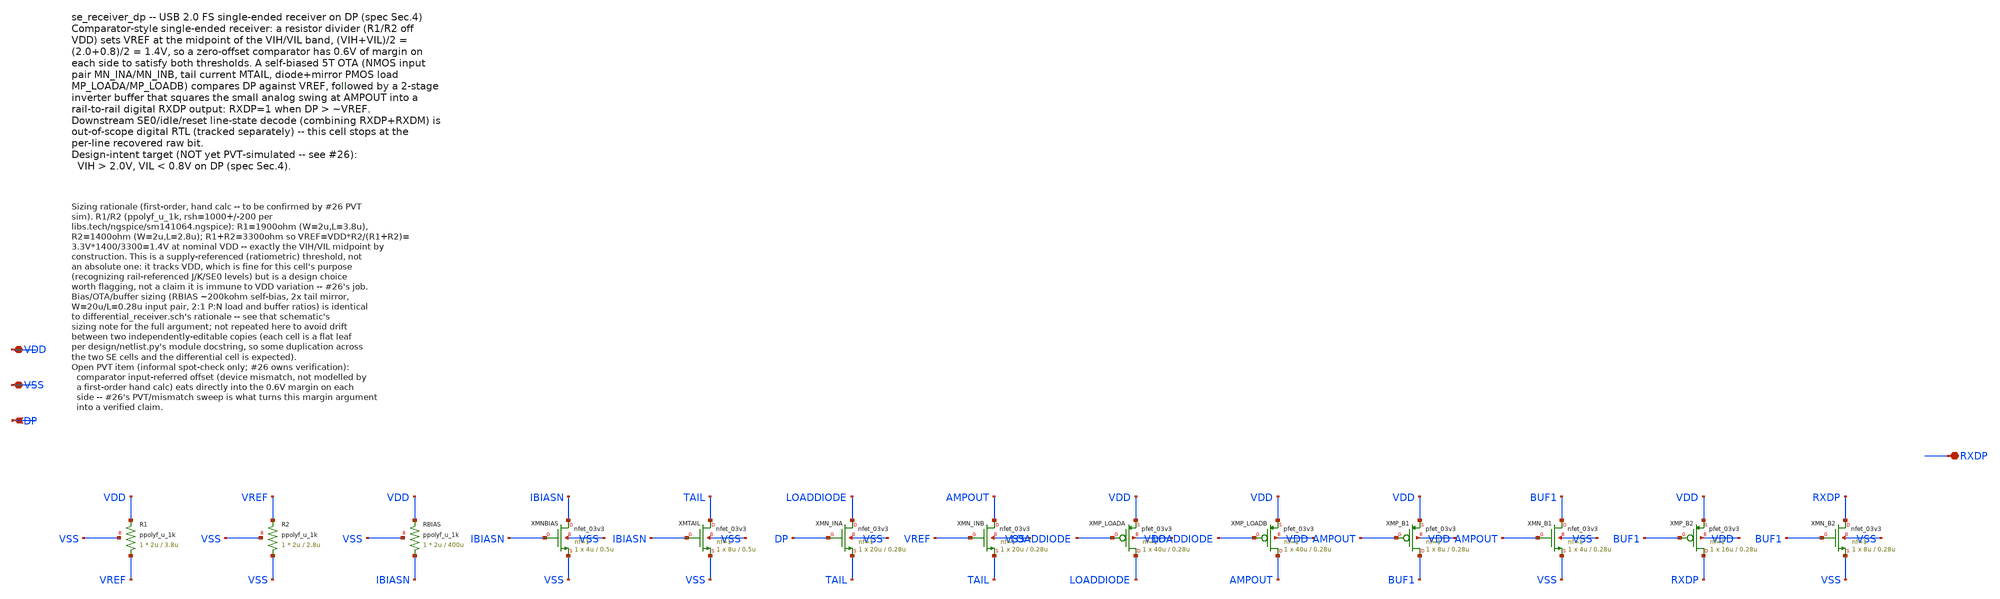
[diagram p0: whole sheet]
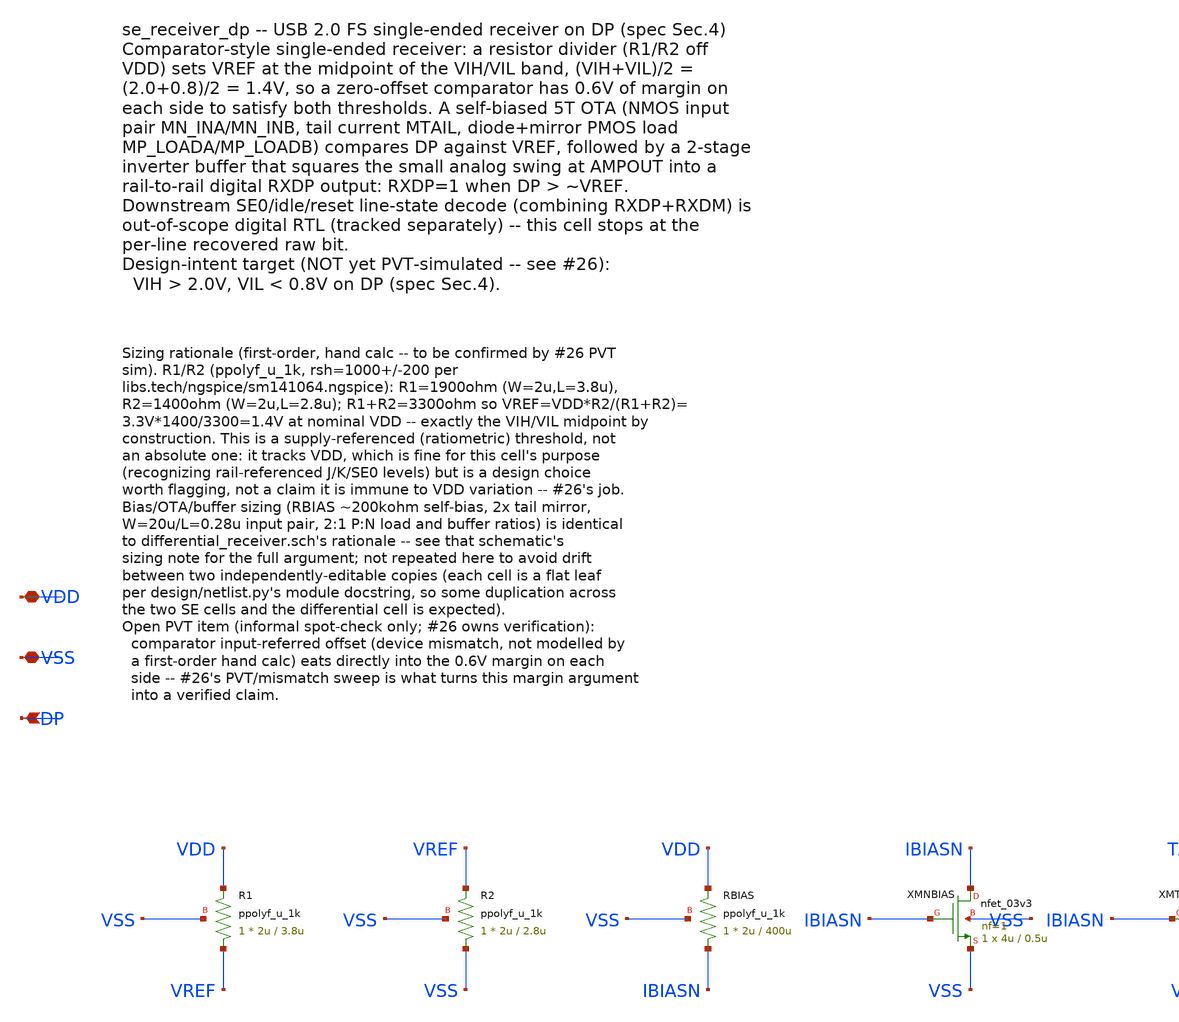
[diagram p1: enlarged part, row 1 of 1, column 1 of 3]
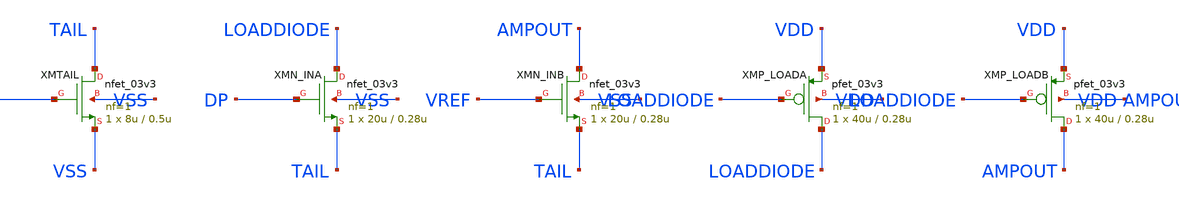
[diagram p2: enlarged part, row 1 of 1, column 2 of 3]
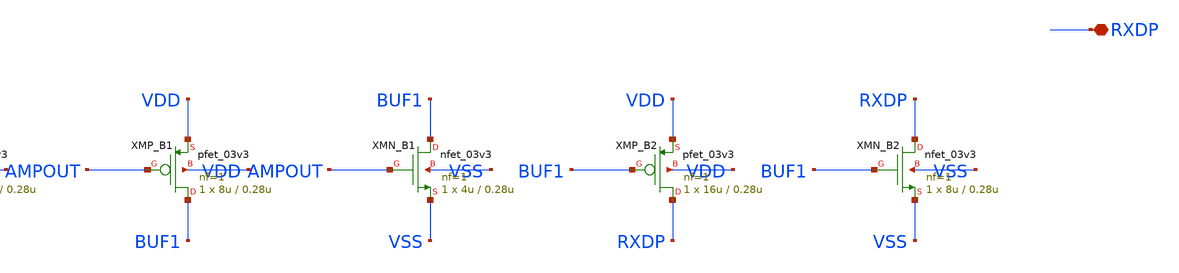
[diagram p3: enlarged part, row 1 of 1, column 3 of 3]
** sch_path: design/se_receiver_dp.sch
**.subckt se_receiver_dp VDD VSS DP RXDP
*.iopin VDD
*.iopin VSS
*.ipin DP
*.iopin RXDP
XR1 VREF VDD VSS ppolyf_u_1k r_width=2u r_length=3.8u m=1
XR2 VSS VREF VSS ppolyf_u_1k r_width=2u r_length=2.8u m=1
XRBIAS IBIASN VDD VSS ppolyf_u_1k r_width=2u r_length=400u m=1
XMNBIAS IBIASN IBIASN VSS VSS nfet_03v3 L=0.5u W=4u nf=1 ad='int((nf+1)/2) * W/nf * 0.18u' as='int((nf+2)/2) * W/nf * 0.18u'
+ pd='2*int((nf+1)/2) * (W/nf + 0.18u)' ps='2*int((nf+2)/2) * (W/nf + 0.18u)' nrd='0.18u / W' nrs='0.18u / W'
+ sa=0 sb=0 sd=0 m=1
XMTAIL TAIL IBIASN VSS VSS nfet_03v3 L=0.5u W=8u nf=1 ad='int((nf+1)/2) * W/nf * 0.18u' as='int((nf+2)/2) * W/nf * 0.18u'
+ pd='2*int((nf+1)/2) * (W/nf + 0.18u)' ps='2*int((nf+2)/2) * (W/nf + 0.18u)' nrd='0.18u / W' nrs='0.18u / W'
+ sa=0 sb=0 sd=0 m=1
XMN_INA LOADDIODE DP TAIL VSS nfet_03v3 L=0.28u W=20u nf=1 ad='int((nf+1)/2) * W/nf * 0.18u' as='int((nf+2)/2) * W/nf * 0.18u'
+ pd='2*int((nf+1)/2) * (W/nf + 0.18u)' ps='2*int((nf+2)/2) * (W/nf + 0.18u)' nrd='0.18u / W' nrs='0.18u / W'
+ sa=0 sb=0 sd=0 m=1
XMN_INB AMPOUT VREF TAIL VSS nfet_03v3 L=0.28u W=20u nf=1 ad='int((nf+1)/2) * W/nf * 0.18u' as='int((nf+2)/2) * W/nf * 0.18u'
+ pd='2*int((nf+1)/2) * (W/nf + 0.18u)' ps='2*int((nf+2)/2) * (W/nf + 0.18u)' nrd='0.18u / W' nrs='0.18u / W'
+ sa=0 sb=0 sd=0 m=1
XMP_LOADA LOADDIODE LOADDIODE VDD VDD pfet_03v3 L=0.28u W=40u nf=1 ad='int((nf+1)/2) * W/nf * 0.18u'
+ as='int((nf+2)/2) * W/nf * 0.18u' pd='2*int((nf+1)/2) * (W/nf + 0.18u)' ps='2*int((nf+2)/2) * (W/nf + 0.18u)'
+ nrd='0.18u / W' nrs='0.18u / W' sa=0 sb=0 sd=0 m=1
XMP_LOADB AMPOUT LOADDIODE VDD VDD pfet_03v3 L=0.28u W=40u nf=1 ad='int((nf+1)/2) * W/nf * 0.18u' as='int((nf+2)/2) * W/nf * 0.18u'
+ pd='2*int((nf+1)/2) * (W/nf + 0.18u)' ps='2*int((nf+2)/2) * (W/nf + 0.18u)' nrd='0.18u / W' nrs='0.18u / W'
+ sa=0 sb=0 sd=0 m=1
XMP_B1 BUF1 AMPOUT VDD VDD pfet_03v3 L=0.28u W=8u nf=1 ad='int((nf+1)/2) * W/nf * 0.18u' as='int((nf+2)/2) * W/nf * 0.18u'
+ pd='2*int((nf+1)/2) * (W/nf + 0.18u)' ps='2*int((nf+2)/2) * (W/nf + 0.18u)' nrd='0.18u / W' nrs='0.18u / W'
+ sa=0 sb=0 sd=0 m=1
XMN_B1 BUF1 AMPOUT VSS VSS nfet_03v3 L=0.28u W=4u nf=1 ad='int((nf+1)/2) * W/nf * 0.18u' as='int((nf+2)/2) * W/nf * 0.18u'
+ pd='2*int((nf+1)/2) * (W/nf + 0.18u)' ps='2*int((nf+2)/2) * (W/nf + 0.18u)' nrd='0.18u / W' nrs='0.18u / W'
+ sa=0 sb=0 sd=0 m=1
XMP_B2 RXDP BUF1 VDD VDD pfet_03v3 L=0.28u W=16u nf=1 ad='int((nf+1)/2) * W/nf * 0.18u' as='int((nf+2)/2) * W/nf * 0.18u'
+ pd='2*int((nf+1)/2) * (W/nf + 0.18u)' ps='2*int((nf+2)/2) * (W/nf + 0.18u)' nrd='0.18u / W' nrs='0.18u / W'
+ sa=0 sb=0 sd=0 m=1
XMN_B2 RXDP BUF1 VSS VSS nfet_03v3 L=0.28u W=8u nf=1 ad='int((nf+1)/2) * W/nf * 0.18u' as='int((nf+2)/2) * W/nf * 0.18u'
+ pd='2*int((nf+1)/2) * (W/nf + 0.18u)' ps='2*int((nf+2)/2) * (W/nf + 0.18u)' nrd='0.18u / W' nrs='0.18u / W'
+ sa=0 sb=0 sd=0 m=1
**.ends
.end
